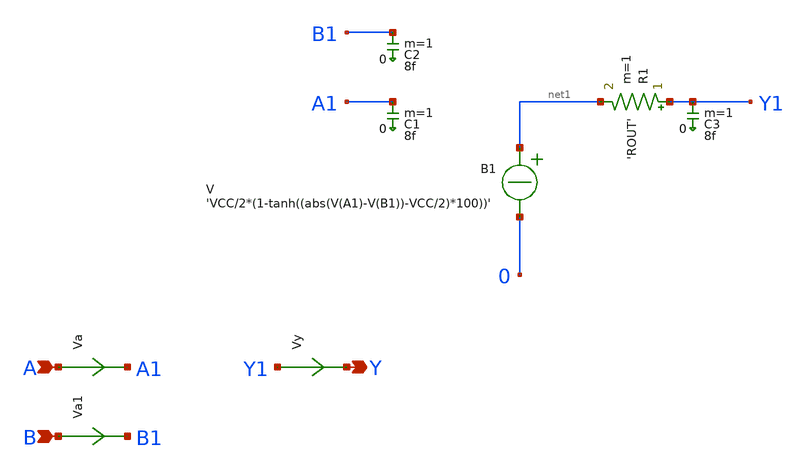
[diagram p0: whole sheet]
** sch_path: xschem_libs_newsym/ngspice/xnor_ngspice/schematic/xnor_ngspice.sch
* Copyright (C) 1998-2024 Stefan Frederik Schippers
* This program is free software; you can redistribute it and/or modify
* it under the terms of the GNU General Public License as published by
* the Free Software Foundation; either version 2 of the License, or
* (at your option) any later version.
* This program is distributed in the hope that it will be useful,
* but WITHOUT ANY WARRANTY; without even the implied warranty of
* MERCHANTABILITY or FITNESS FOR A PARTICULAR PURPOSE.  See the
* GNU General Public License for more details.
* You should have received a copy of the GNU General Public License
* along with this program; if not, write to the Free Software
**.subckt xnor_ngspice A Y B
*.ipin A
*.opin Y
*.ipin B
B1 net1 0 V = 'VCC/2*(1-tanh((abs(V(A1)-V(B1))-VCC/2)*100))'
R1 Y1 net1 'ROUT' m=1
Va A A1 0
.save i(va)
Vy Y1 Y 0
.save i(vy)
Va1 B B1 0
.save i(va1)
C1 A1 0 8f m=1
C2 B1 0 8f m=1
C3 Y1 0 8f m=1
**.ends
.end
